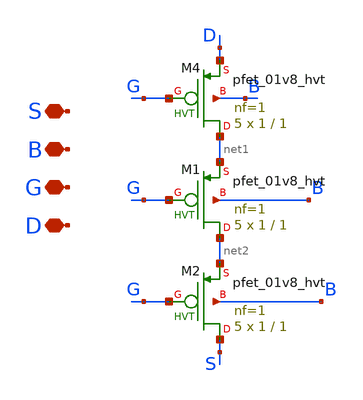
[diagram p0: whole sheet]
** sch_path: xschem/INA/Transistors/transistors_bias_network/nfet_m16.sch
**.subckt nfet_m16 S B G D
*.iopin S
*.iopin B
*.iopin G
*.iopin D
XM4 net1 G D B sky130_fd_pr__pfet_01v8_hvt L=1 W=1 nf=1 ad='int((nf+1)/2) * W/nf * 0.29' as='int((nf+2)/2) * W/nf * 0.29'
+ pd='2*int((nf+1)/2) * (W/nf + 0.29)' ps='2*int((nf+2)/2) * (W/nf + 0.29)' nrd='0.29 / W' nrs='0.29 / W'
+ sa=0 sb=0 sd=0 mult=5 m=5
XM1 net2 G net1 B sky130_fd_pr__pfet_01v8_hvt L=1 W=1 nf=1 ad='int((nf+1)/2) * W/nf * 0.29' as='int((nf+2)/2) * W/nf * 0.29'
+ pd='2*int((nf+1)/2) * (W/nf + 0.29)' ps='2*int((nf+2)/2) * (W/nf + 0.29)' nrd='0.29 / W' nrs='0.29 / W'
+ sa=0 sb=0 sd=0 mult=5 m=5
XM2 S G net2 B sky130_fd_pr__pfet_01v8_hvt L=1 W=1 nf=1 ad='int((nf+1)/2) * W/nf * 0.29' as='int((nf+2)/2) * W/nf * 0.29'
+ pd='2*int((nf+1)/2) * (W/nf + 0.29)' ps='2*int((nf+2)/2) * (W/nf + 0.29)' nrd='0.29 / W' nrs='0.29 / W'
+ sa=0 sb=0 sd=0 mult=5 m=5
**.ends
.end
